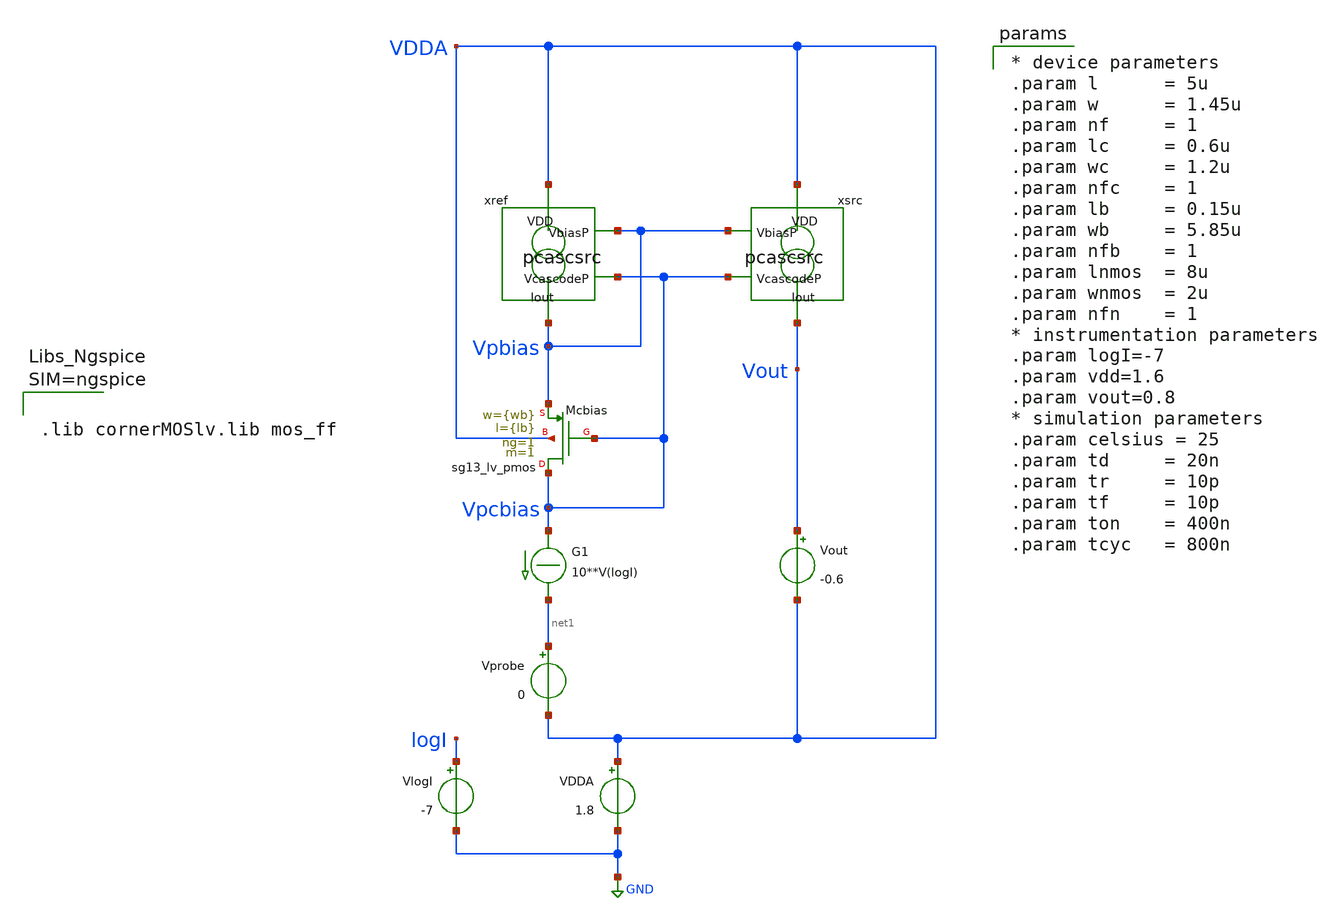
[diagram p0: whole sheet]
** sch_path: xschem/test_pcascsrc_DC.sch
**.subckt test_pcascsrc_DC
Vout Vout VDDA -0.6
.save i(vout)
Vprobe net1 VDDA 0
.save i(vprobe)
G1 Vpcbias net1 CUR=' 10**V(logI) '
VlogI logI GND -7
.save i(vlogi)
xref VDDA Vpbias Vpcbias Vpbias pcascsrc l={l} w={w} lc={lc} wc={wc}
xsrc VDDA Vpbias Vpcbias Vout pcascsrc l={l} w={w} lc={lc} wc={wc}
VDDA VDDA GND 1.8
.save i(vdda)
XMcbias Vpcbias Vpcbias Vpbias VDDA sg13_lv_pmos w={wb} l={lb} ng=1 m=1 mm_ok=1
**** begin user architecture code


.include test_pcascsrc_DC.save
.temp=27
.options savecurrents
.control
save all
op
write test_pcascsrc_DC.raw
set appendwrite
dc Vout 0 -1.8 -10m VlogI -8 -6 0.5
write test_pcascsrc_DC.raw
plot title 'voltages' vdda vpbias vpcbias vout xref.drain xsrc.drain
plot title 'gm/Id' @n.xref.xmsrc.nsg13_lv_pmos[gm]/vprobe#branch @n.xref.xmcasc.nsg13_lv_pmos[gm]/vprobe#branch
+ @n.xsrc.xmsrc.nsg13_lv_pmos[gm]/vout#branch @n.xsrc.xmcasc.nsg13_lv_pmos[gm]/vout#branch
plot title 'gm/gds' @n.xref.xmsrc.nsg13_lv_pmos[gm]/@n.xref.xmsrc.nsg13_lv_pmos[gds] @n.xref.xmcasc.nsg13_lv_pmos[gm]/@n.xref.xmcasc.nsg13_lv_pmos[gds]
+ @n.xsrc.xmsrc.nsg13_lv_pmos[gm]/@n.xsrc.xmsrc.nsg13_lv_pmos[gds] @n.xsrc.xmcasc.nsg13_lv_pmos[gm]/@n.xsrc.xmcasc.nsg13_lv_pmos[gds]
plot title 'Vth' @n.xref.xmsrc.nsg13_lv_pmos[vth] @n.xref.xmcasc.nsg13_lv_pmos[vth] @n.xsrc.xmsrc.nsg13_lv_pmos[vth]
+ @n.xsrc.xmcasc.nsg13_lv_pmos[vth]
plot title 'output/reference current asymmetry' ylimit -2m 2m 2*(vout#branch-vprobe#branch)/(vprobe#branch+vout#branch)
.endc





.lib cornerMOSlv.lib mos_ff




* device parameters
.param l      = 5u
.param w      = 1.45u
.param nf     = 1
.param lc     = 0.6u
.param wc     = 1.2u
.param nfc    = 1
.param lb     = 0.15u
.param wb     = 5.85u
.param nfb    = 1
.param lnmos  = 8u
.param wnmos  = 2u
.param nfn    = 1
* instrumentation parameters
.param logI=-7
.param vdd=1.6
.param vout=0.8
* simulation parameters
.param celsius = 25
.param td     = 20n
.param tr     = 10p
.param tf     = 10p
.param ton    = 400n
.param tcyc   = 800n


**** end user architecture code
**.ends

* expanding   symbol:  pcascsrc.sym # of pins=4
** sym_path: xschem/pcascsrc.sym
** sch_path: xschem/pcascsrc.sch
.subckt pcascsrc VDD VbiasP VcascodeP Iout  l=2u w=.74u lc=.3u wc=.3u
*.ipin VcascodeP
*.ipin VbiasP
*.opin Iout
*.ipin VDD
XMsrc drain VbiasP VDD VDD sg13_lv_pmos w={w} l={l} ng=1 m=1 mm_ok=1
XMcasc Iout VcascodeP drain VDD sg13_lv_pmos w={wc} l={lc} ng=1 m=1 mm_ok=1
.ends

.GLOBAL GND
.end
